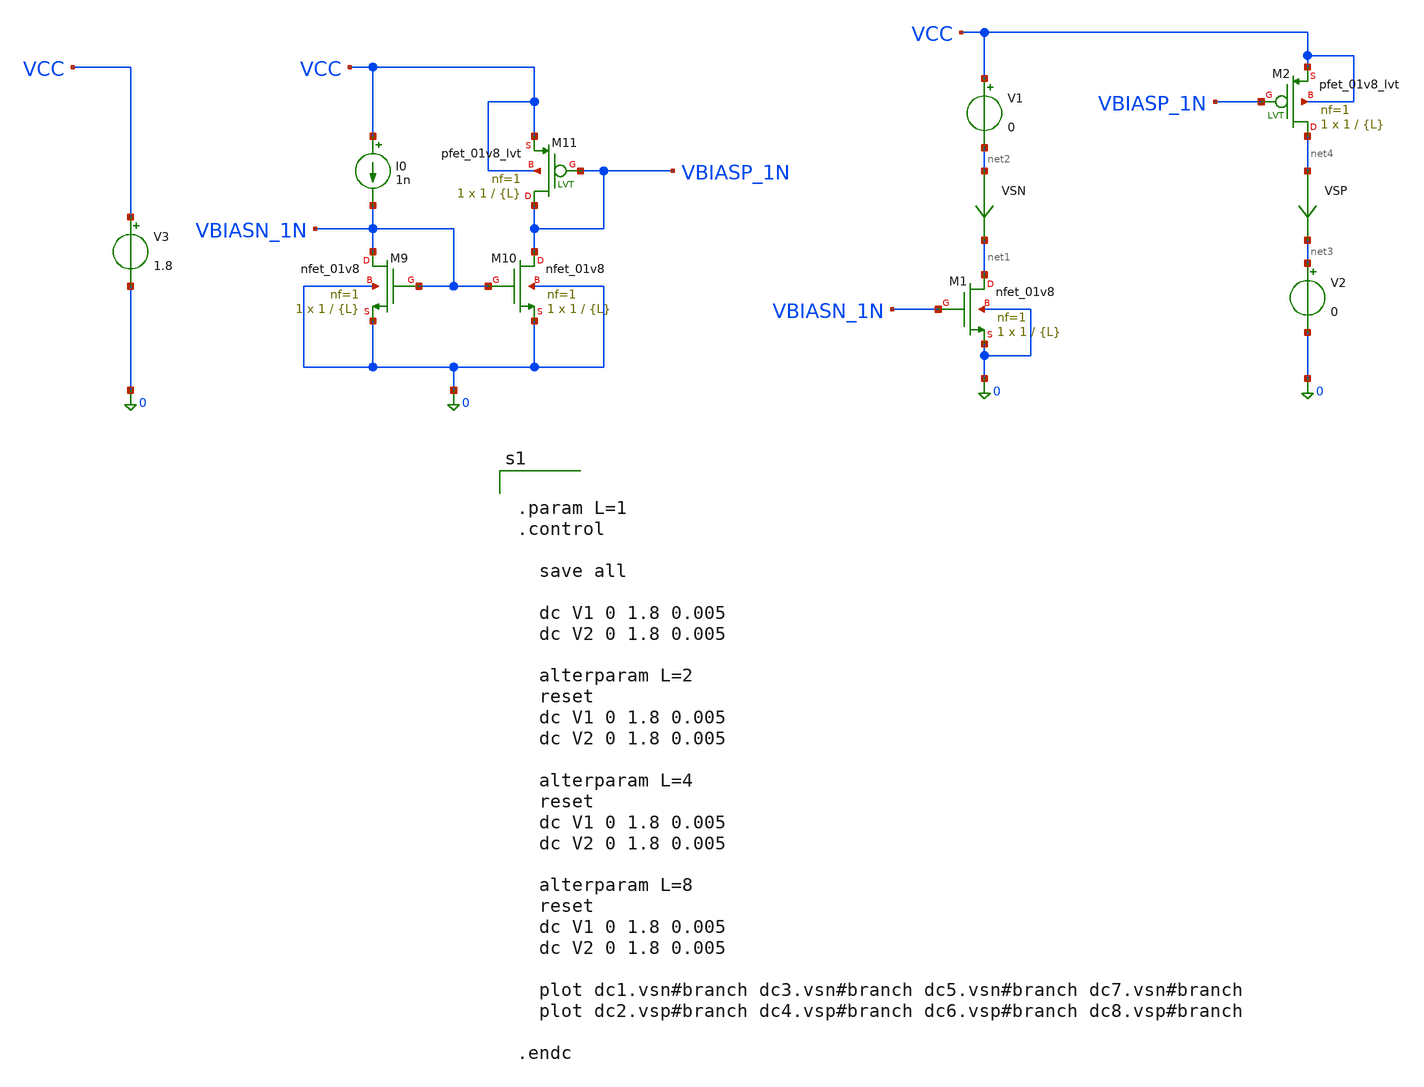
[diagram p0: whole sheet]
** sch_path: schem/bias/bias_lvt_tb.sch
**.subckt bias_lvt_tb
I0 VCC VBIASN_1N 1n
XM9 VBIASN_1N VBIASN_1N 0 0 sky130_fd_pr__nfet_01v8 L={L} W=1 nf=1 ad='int((1 + 1)/2) * 1 / 1 * 0.29'
+ as='int((1 + 2)/2) * 1 / 1 * 0.29' pd='2*int((1 + 1)/2) * (1 / 1 + 0.29)' ps='2*int((1 + 2)/2) * (1 / 1 + 0.29)'
+ nrd='0.29 / 1 ' nrs='0.29 / 1 ' sa=0 sb=0 sd=0 mult=1 m=1
XM10 VBIASP_1N VBIASN_1N 0 0 sky130_fd_pr__nfet_01v8 L={L} W=1 nf=1 ad='int((1 + 1)/2) * 1 / 1 * 0.29'
+ as='int((1 + 2)/2) * 1 / 1 * 0.29' pd='2*int((1 + 1)/2) * (1 / 1 + 0.29)' ps='2*int((1 + 2)/2) * (1 / 1 + 0.29)'
+ nrd='0.29 / 1 ' nrs='0.29 / 1 ' sa=0 sb=0 sd=0 mult=1 m=1
XM11 VBIASP_1N VBIASP_1N VCC VCC sky130_fd_pr__pfet_01v8_lvt L={L} W=1 nf=1 ad='int((1 + 1)/2) * 1 / 1 * 0.29'
+ as='int((1 + 2)/2) * 1 / 1 * 0.29' pd='2*int((1 + 1)/2) * (1 / 1 + 0.29)' ps='2*int((1 + 2)/2) * (1 / 1 + 0.29)'
+ nrd='0.29 / 1 ' nrs='0.29 / 1 ' sa=0 sb=0 sd=0 mult=1 m=1
XM1 net1 VBIASN_1N 0 0 sky130_fd_pr__nfet_01v8 L={L} W=1 nf=1 ad='int((1 + 1)/2) * 1 / 1 * 0.29' as='int((1 + 2)/2) * 1 / 1 * 0.29'
+ pd='2*int((1 + 1)/2) * (1 / 1 + 0.29)' ps='2*int((1 + 2)/2) * (1 / 1 + 0.29)' nrd='0.29 / 1 ' nrs='0.29 / 1 '
+ sa=0 sb=0 sd=0 mult=1 m=1
VSN net2 net1 0
.save i(vsn)
V1 VCC net2 0
XM2 net4 VBIASP_1N VCC VCC sky130_fd_pr__pfet_01v8_lvt L={L} W=1 nf=1 ad='int((1 + 1)/2) * 1 / 1 * 0.29'
+ as='int((1 + 2)/2) * 1 / 1 * 0.29' pd='2*int((1 + 1)/2) * (1 / 1 + 0.29)' ps='2*int((1 + 2)/2) * (1 / 1 + 0.29)'
+ nrd='0.29 / 1 ' nrs='0.29 / 1 ' sa=0 sb=0 sd=0 mult=1 m=1
VSP net4 net3 0
.save i(vsp)
V2 net3 0 0
V3 VCC 0 1.8
**** begin user architecture code

** opencircuitdesign pdks install
.lib $::SKYWATER_MODELS/sky130.lib.spice tt



.param L=1
.control

  save all

  dc V1 0 1.8 0.005
  dc V2 0 1.8 0.005

  alterparam L=2
  reset
  dc V1 0 1.8 0.005
  dc V2 0 1.8 0.005

  alterparam L=4
  reset
  dc V1 0 1.8 0.005
  dc V2 0 1.8 0.005

  alterparam L=8
  reset
  dc V1 0 1.8 0.005
  dc V2 0 1.8 0.005

  plot dc1.vsn#branch dc3.vsn#branch dc5.vsn#branch dc7.vsn#branch
  plot dc2.vsp#branch dc4.vsp#branch dc6.vsp#branch dc8.vsp#branch

.endc


**** end user architecture code
**.ends
.end
